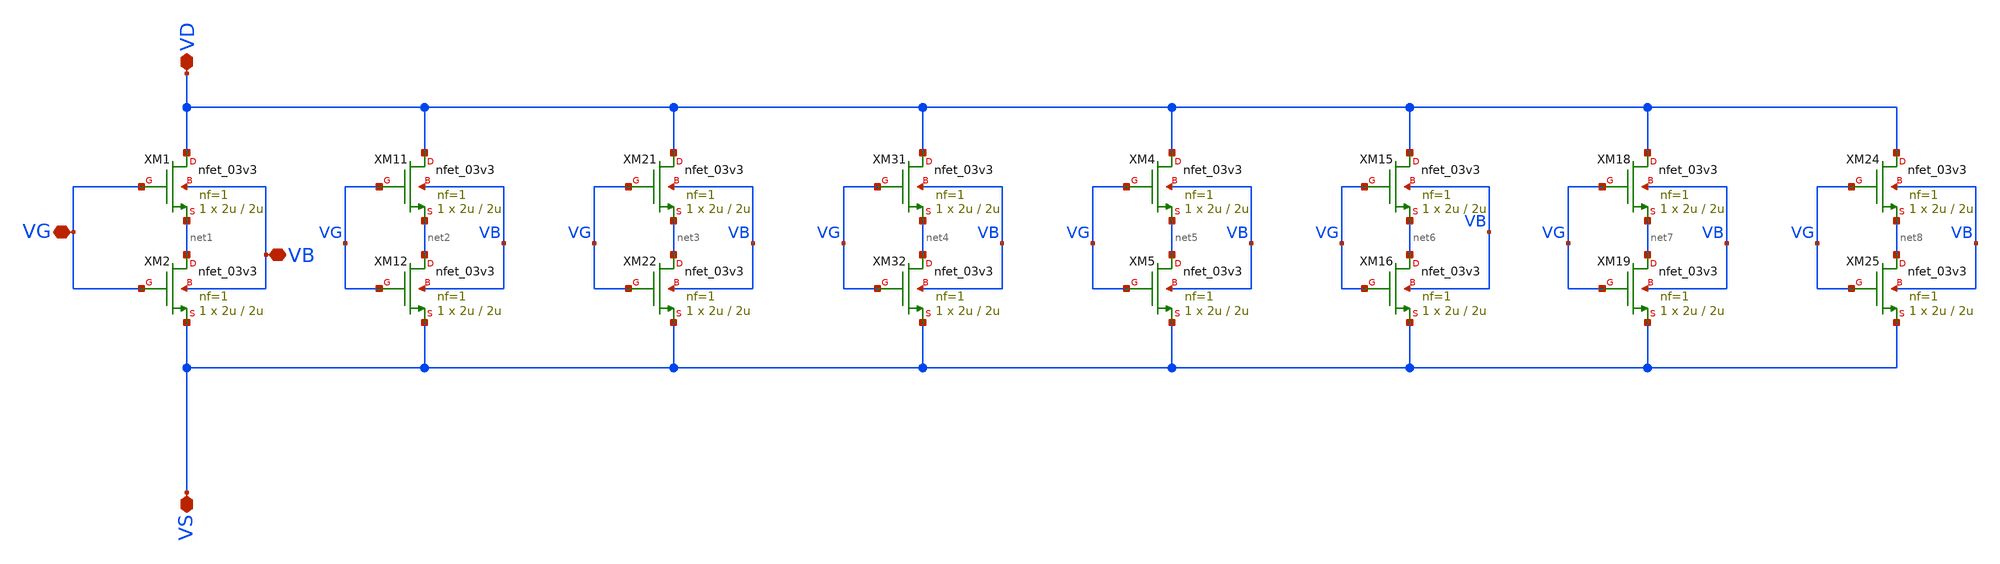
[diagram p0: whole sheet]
** sch_path: Voltage_Reference/symbols_vr/NMOS_association_18u_5u.sch
**.subckt NMOS_association_18u_5u VD VG VS VB
*.iopin VD
*.iopin VG
*.iopin VS
*.iopin VB
XM1 VD VG net1 VB nfet_03v3 L=2u W=2u nf=1 ad='int((nf+1)/2) * W/nf * 0.18u' as='int((nf+2)/2) * W/nf * 0.18u'
+ pd='2*int((nf+1)/2) * (W/nf + 0.18u)' ps='2*int((nf+2)/2) * (W/nf + 0.18u)' nrd='0.18u / W' nrs='0.18u / W'
+ sa=0 sb=0 sd=0 m=1
XM2 net1 VG VS VB nfet_03v3 L=2u W=2u nf=1 ad='int((nf+1)/2) * W/nf * 0.18u' as='int((nf+2)/2) * W/nf * 0.18u'
+ pd='2*int((nf+1)/2) * (W/nf + 0.18u)' ps='2*int((nf+2)/2) * (W/nf + 0.18u)' nrd='0.18u / W' nrs='0.18u / W'
+ sa=0 sb=0 sd=0 m=1
XM11 VD VG net2 VB nfet_03v3 L=2u W=2u nf=1 ad='int((nf+1)/2) * W/nf * 0.18u' as='int((nf+2)/2) * W/nf * 0.18u'
+ pd='2*int((nf+1)/2) * (W/nf + 0.18u)' ps='2*int((nf+2)/2) * (W/nf + 0.18u)' nrd='0.18u / W' nrs='0.18u / W'
+ sa=0 sb=0 sd=0 m=1
XM12 net2 VG VS VB nfet_03v3 L=2u W=2u nf=1 ad='int((nf+1)/2) * W/nf * 0.18u' as='int((nf+2)/2) * W/nf * 0.18u'
+ pd='2*int((nf+1)/2) * (W/nf + 0.18u)' ps='2*int((nf+2)/2) * (W/nf + 0.18u)' nrd='0.18u / W' nrs='0.18u / W'
+ sa=0 sb=0 sd=0 m=1
XM21 VD VG net3 VB nfet_03v3 L=2u W=2u nf=1 ad='int((nf+1)/2) * W/nf * 0.18u' as='int((nf+2)/2) * W/nf * 0.18u'
+ pd='2*int((nf+1)/2) * (W/nf + 0.18u)' ps='2*int((nf+2)/2) * (W/nf + 0.18u)' nrd='0.18u / W' nrs='0.18u / W'
+ sa=0 sb=0 sd=0 m=1
XM22 net3 VG VS VB nfet_03v3 L=2u W=2u nf=1 ad='int((nf+1)/2) * W/nf * 0.18u' as='int((nf+2)/2) * W/nf * 0.18u'
+ pd='2*int((nf+1)/2) * (W/nf + 0.18u)' ps='2*int((nf+2)/2) * (W/nf + 0.18u)' nrd='0.18u / W' nrs='0.18u / W'
+ sa=0 sb=0 sd=0 m=1
XM31 VD VG net4 VB nfet_03v3 L=2u W=2u nf=1 ad='int((nf+1)/2) * W/nf * 0.18u' as='int((nf+2)/2) * W/nf * 0.18u'
+ pd='2*int((nf+1)/2) * (W/nf + 0.18u)' ps='2*int((nf+2)/2) * (W/nf + 0.18u)' nrd='0.18u / W' nrs='0.18u / W'
+ sa=0 sb=0 sd=0 m=1
XM32 net4 VG VS VB nfet_03v3 L=2u W=2u nf=1 ad='int((nf+1)/2) * W/nf * 0.18u' as='int((nf+2)/2) * W/nf * 0.18u'
+ pd='2*int((nf+1)/2) * (W/nf + 0.18u)' ps='2*int((nf+2)/2) * (W/nf + 0.18u)' nrd='0.18u / W' nrs='0.18u / W'
+ sa=0 sb=0 sd=0 m=1
XM4 VD VG net5 VB nfet_03v3 L=2u W=2u nf=1 ad='int((nf+1)/2) * W/nf * 0.18u' as='int((nf+2)/2) * W/nf * 0.18u'
+ pd='2*int((nf+1)/2) * (W/nf + 0.18u)' ps='2*int((nf+2)/2) * (W/nf + 0.18u)' nrd='0.18u / W' nrs='0.18u / W'
+ sa=0 sb=0 sd=0 m=1
XM5 net5 VG VS VB nfet_03v3 L=2u W=2u nf=1 ad='int((nf+1)/2) * W/nf * 0.18u' as='int((nf+2)/2) * W/nf * 0.18u'
+ pd='2*int((nf+1)/2) * (W/nf + 0.18u)' ps='2*int((nf+2)/2) * (W/nf + 0.18u)' nrd='0.18u / W' nrs='0.18u / W'
+ sa=0 sb=0 sd=0 m=1
XM15 VD VG net6 VB nfet_03v3 L=2u W=2u nf=1 ad='int((nf+1)/2) * W/nf * 0.18u' as='int((nf+2)/2) * W/nf * 0.18u'
+ pd='2*int((nf+1)/2) * (W/nf + 0.18u)' ps='2*int((nf+2)/2) * (W/nf + 0.18u)' nrd='0.18u / W' nrs='0.18u / W'
+ sa=0 sb=0 sd=0 m=1
XM16 net6 VG VS VB nfet_03v3 L=2u W=2u nf=1 ad='int((nf+1)/2) * W/nf * 0.18u' as='int((nf+2)/2) * W/nf * 0.18u'
+ pd='2*int((nf+1)/2) * (W/nf + 0.18u)' ps='2*int((nf+2)/2) * (W/nf + 0.18u)' nrd='0.18u / W' nrs='0.18u / W'
+ sa=0 sb=0 sd=0 m=1
XM18 VD VG net7 VB nfet_03v3 L=2u W=2u nf=1 ad='int((nf+1)/2) * W/nf * 0.18u' as='int((nf+2)/2) * W/nf * 0.18u'
+ pd='2*int((nf+1)/2) * (W/nf + 0.18u)' ps='2*int((nf+2)/2) * (W/nf + 0.18u)' nrd='0.18u / W' nrs='0.18u / W'
+ sa=0 sb=0 sd=0 m=1
XM19 net7 VG VS VB nfet_03v3 L=2u W=2u nf=1 ad='int((nf+1)/2) * W/nf * 0.18u' as='int((nf+2)/2) * W/nf * 0.18u'
+ pd='2*int((nf+1)/2) * (W/nf + 0.18u)' ps='2*int((nf+2)/2) * (W/nf + 0.18u)' nrd='0.18u / W' nrs='0.18u / W'
+ sa=0 sb=0 sd=0 m=1
XM24 VD VG net8 VB nfet_03v3 L=2u W=2u nf=1 ad='int((nf+1)/2) * W/nf * 0.18u' as='int((nf+2)/2) * W/nf * 0.18u'
+ pd='2*int((nf+1)/2) * (W/nf + 0.18u)' ps='2*int((nf+2)/2) * (W/nf + 0.18u)' nrd='0.18u / W' nrs='0.18u / W'
+ sa=0 sb=0 sd=0 m=1
XM25 net8 VG VS VB nfet_03v3 L=2u W=2u nf=1 ad='int((nf+1)/2) * W/nf * 0.18u' as='int((nf+2)/2) * W/nf * 0.18u'
+ pd='2*int((nf+1)/2) * (W/nf + 0.18u)' ps='2*int((nf+2)/2) * (W/nf + 0.18u)' nrd='0.18u / W' nrs='0.18u / W'
+ sa=0 sb=0 sd=0 m=1
**.ends
.end
